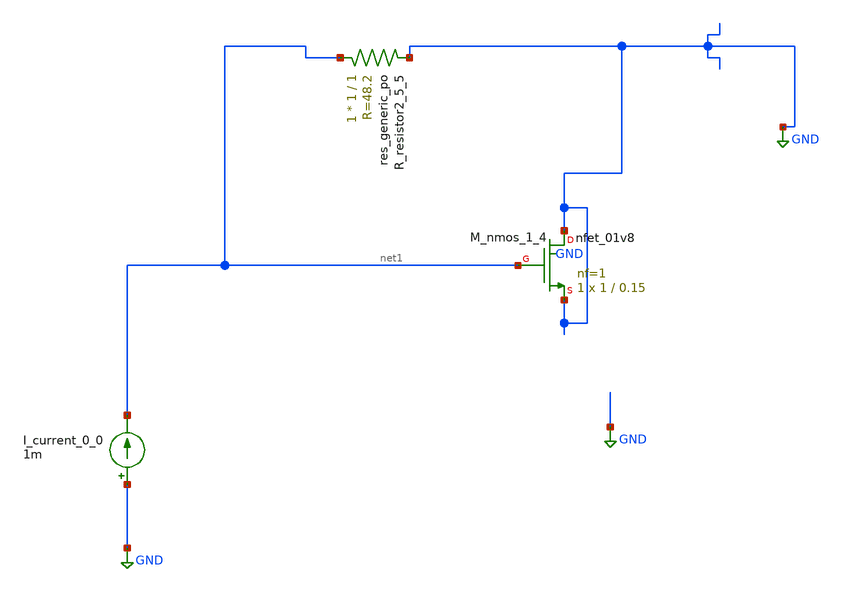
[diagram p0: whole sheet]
** sch_path: schematics/AMSNet/449.sch
**.subckt 449
I_current_0_0 GND net1 1m
XM_nmos_1_4 GND net1 GND GND sky130_fd_pr__nfet_01v8 L=0.15 W=1 nf=1 ad='int((1 + 1)/2) * 1 / 1 * 0.29'
+ as='int((1 + 2)/2) * 1 / 1 * 0.29' pd='2*int((1 + 1)/2) * (1 / 1 + 0.29)' ps='2*int((1 + 2)/2) * (1 / 1 + 0.29)'
+ nrd='0.29 / 1 ' nrs='0.29 / 1 ' sa=0 sb=0 sd=0 mult=1 m=1
XR_resistor2_5_5 net1 GND sky130_fd_pr__res_generic_po W=1 L=1 m=1
**.ends
.GLOBAL GND
.end
